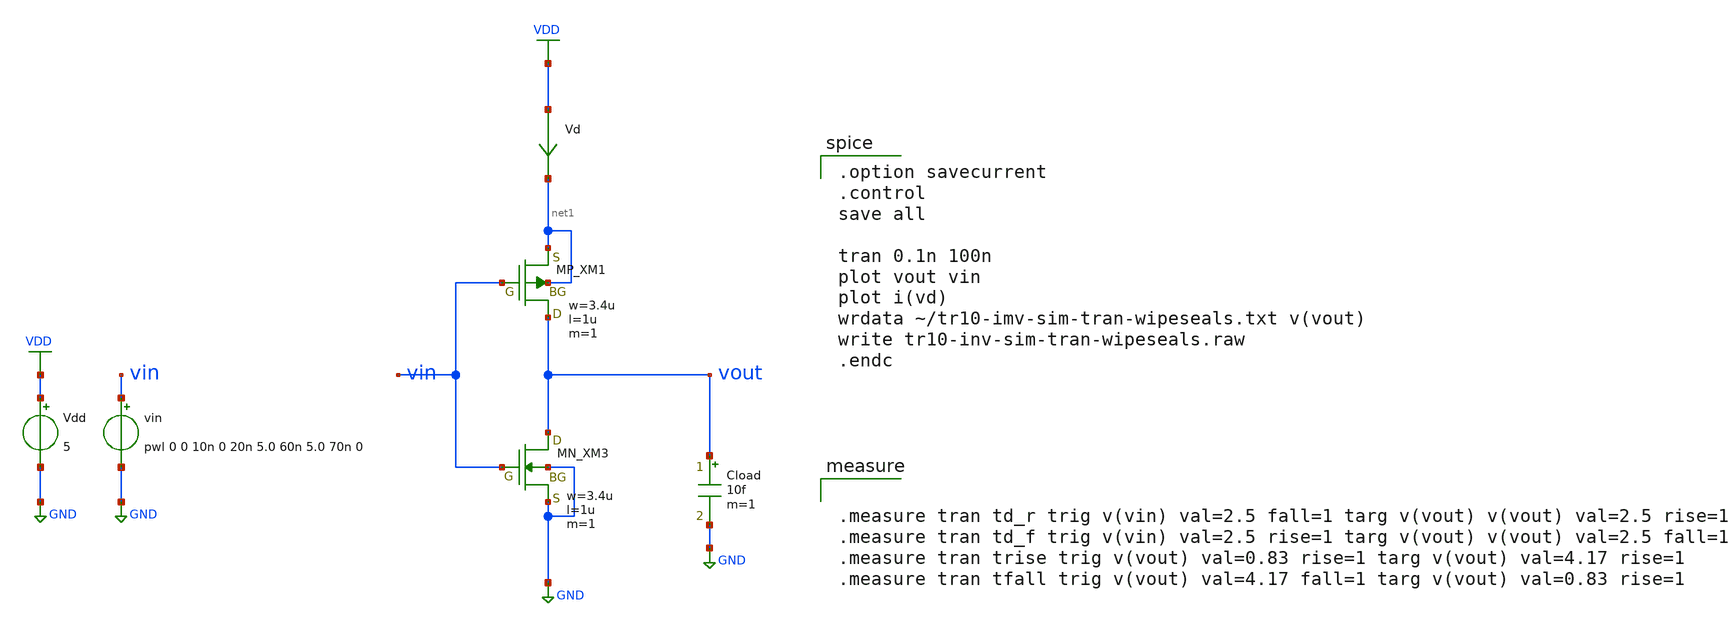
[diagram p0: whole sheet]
** sch_path: member_project/inverter/wipeseals/misc/tr10-inv-sim-tran-wipeseals.sch
**.subckt tr10-inv-sim-tran-wipeseals
Vdd VDD GND 5
vin vin GND pwl 0 0 10n 0 20n 5.0 60n 5.0 70n 0
Vd VDD net1 0
.save i(vd)
Cload vout GND 10f m=1
XM1 vout vin net1 net1 PMOS w=3.4u l=1u as=0 ad=0 ps=0 pd=0 nrd=0 nrs=0 m=1
XM3 vout vin GND GND NMOS w=3.4u l=1u as=0 ad=0 ps=0 pd=0 nrd=0 nrs=0 m=1
**** begin user architecture code
 .include $::LIB/../ip62_models

.option savecurrent
.control
save all

tran 0.1n 100n
plot vout vin
plot i(vd)
wrdata ~/tr10-imv-sim-tran-wipeseals.txt v(vout)
write tr10-inv-sim-tran-wipeseals.raw
.endc




.measure tran td_r trig v(vin) val=2.5 fall=1 targ v(vout) v(vout) val=2.5 rise=1
.measure tran td_f trig v(vin) val=2.5 rise=1 targ v(vout) v(vout) val=2.5 fall=1
.measure tran trise trig v(vout) val=0.83 rise=1 targ v(vout) val=4.17 rise=1
.measure tran tfall trig v(vout) val=4.17 fall=1 targ v(vout) val=0.83 rise=1


**** end user architecture code
**.ends
.GLOBAL VDD
.GLOBAL GND
.end
